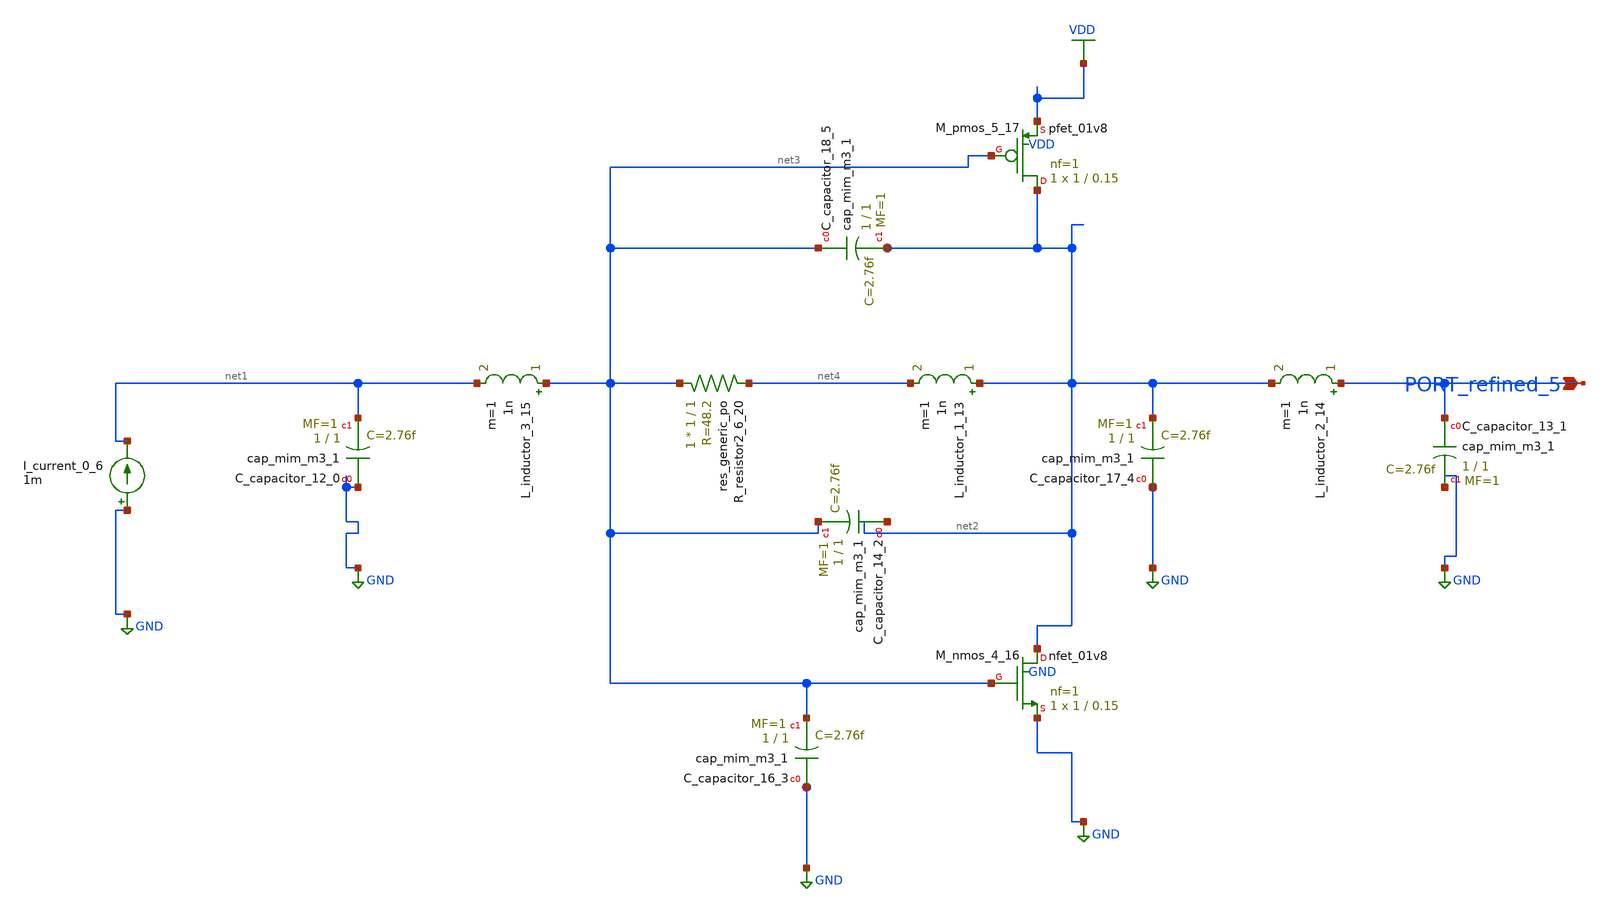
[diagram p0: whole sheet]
** sch_path: schematics/10_1109_OJCAS_2022_3164396_02_001_crop2.sch
**.subckt 10_1109_OJCAS_2022_3164396_02_001_crop2 PORT_refined_5
*.ipin PORT_refined_5
XC_capacitor_12_0 GND net1 sky130_fd_pr__cap_mim_m3_1 W=1 L=1 MF=1 m=1
XC_capacitor_13_1 PORT_refined_5 GND sky130_fd_pr__cap_mim_m3_1 W=1 L=1 MF=1 m=1
XC_capacitor_14_2 net2 net3 sky130_fd_pr__cap_mim_m3_1 W=1 L=1 MF=1 m=1
XC_capacitor_16_3 GND net3 sky130_fd_pr__cap_mim_m3_1 W=1 L=1 MF=1 m=1
XC_capacitor_17_4 GND net2 sky130_fd_pr__cap_mim_m3_1 W=1 L=1 MF=1 m=1
XC_capacitor_18_5 net3 net2 sky130_fd_pr__cap_mim_m3_1 W=1 L=1 MF=1 m=1
I_current_0_6 GND net1 1m
L_inductor_1_13 net2 net4 1n m=1
L_inductor_2_14 PORT_refined_5 net2 1n m=1
L_inductor_3_15 net3 net1 1n m=1
XM_nmos_4_16 net2 net3 GND GND sky130_fd_pr__nfet_01v8 L=0.15 W=1 nf=1 ad='int((1 + 1)/2) * 1 / 1 * 0.29'
+ as='int((1 + 2)/2) * 1 / 1 * 0.29' pd='2*int((1 + 1)/2) * (1 / 1 + 0.29)' ps='2*int((1 + 2)/2) * (1 / 1 + 0.29)'
+ nrd='0.29 / 1 ' nrs='0.29 / 1 ' sa=0 sb=0 sd=0 mult=1 m=1
XM_pmos_5_17 net2 net3 VDD VDD sky130_fd_pr__pfet_01v8 L=0.15 W=1 nf=1 ad='int((1 + 1)/2) * 1 / 1 * 0.29'
+ as='int((1 + 2)/2) * 1 / 1 * 0.29' pd='2*int((1 + 1)/2) * (1 / 1 + 0.29)' ps='2*int((1 + 2)/2) * (1 / 1 + 0.29)'
+ nrd='0.29 / 1 ' nrs='0.29 / 1 ' sa=0 sb=0 sd=0 mult=1 m=1
XR_resistor2_6_20 net3 net4 sky130_fd_pr__res_generic_po W=1 L=1 m=1
**.ends
.GLOBAL GND
.GLOBAL VDD
.end
